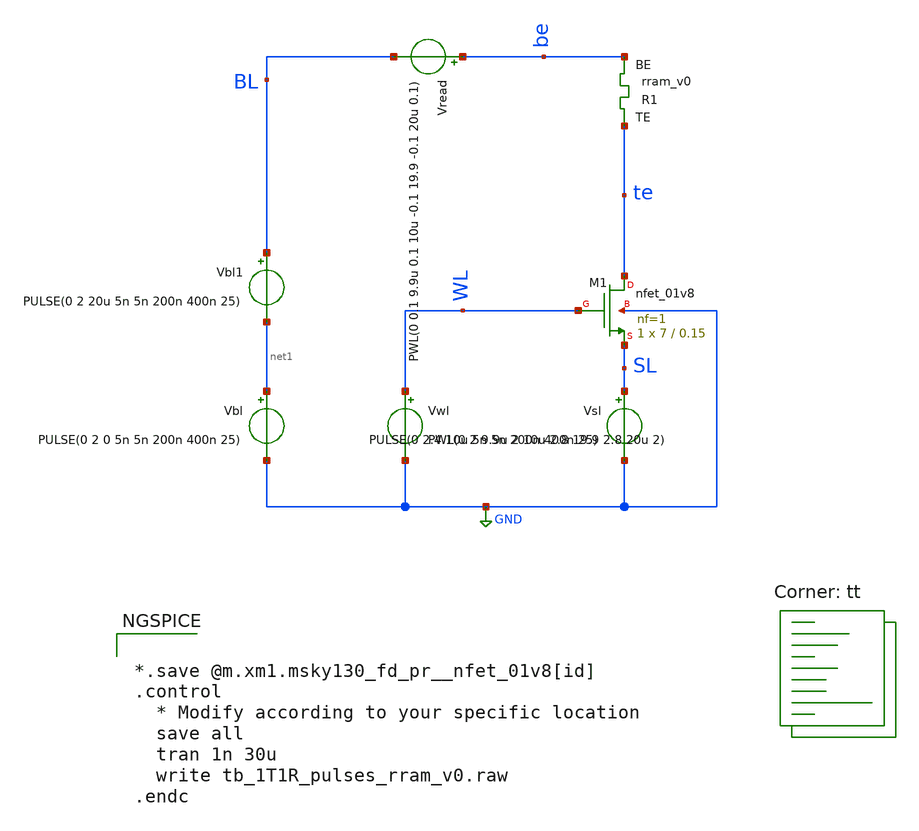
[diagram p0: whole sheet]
** sch_path: memristor_models/wellposed/tb_1T1R_pulses_rram_v0.sch
**.subckt tb_1T1R_pulses_rram_v0
XM1 te WL SL GND sky130_fd_pr__nfet_01v8 L=0.15 W=7 nf=1 ad='int((nf+1)/2) * W/nf * 0.29' as='int((nf+2)/2) * W/nf * 0.29'
+ pd='2*int((nf+1)/2) * (W/nf + 0.29)' ps='2*int((nf+2)/2) * (W/nf + 0.29)' nrd='0.29 / W' nrs='0.29 / W'
+ sa=0 sb=0 sd=0 mult=1 m=1
Vwl WL GND PWL(0 2 9.9u 2 10u 2.8 19.9 2.8 20u 2)
Vbl net1 GND PULSE(0 2 0 5n 5n 200n 400n 25)
Vread be BL PWL(0 0.1 9.9u 0.1 10u -0.1 19.9 -0.1 20u 0.1)
XR1 te be rram_v0
Vsl SL GND PULSE(0 2.4 10u 5n 5n 200n 400n 25)
Vbl1 BL net1 PULSE(0 2 20u 5n 5n 200n 400n 25)
**** begin user architecture code


*.save @m.xm1.msky130_fd_pr__nfet_01v8[id]
.control
  * Modify according to your specific location
  save all
  tran 1n 30u
  write tb_1T1R_pulses_rram_v0.raw
.endc



.lib $::SKYWATER_MODELS/sky130.lib.spice tt

** opencircuitdesign pdks install
.inc $::SKYWATER_MODELS/rram_v0.spice

**** end user architecture code
**.ends
.GLOBAL GND
.end
